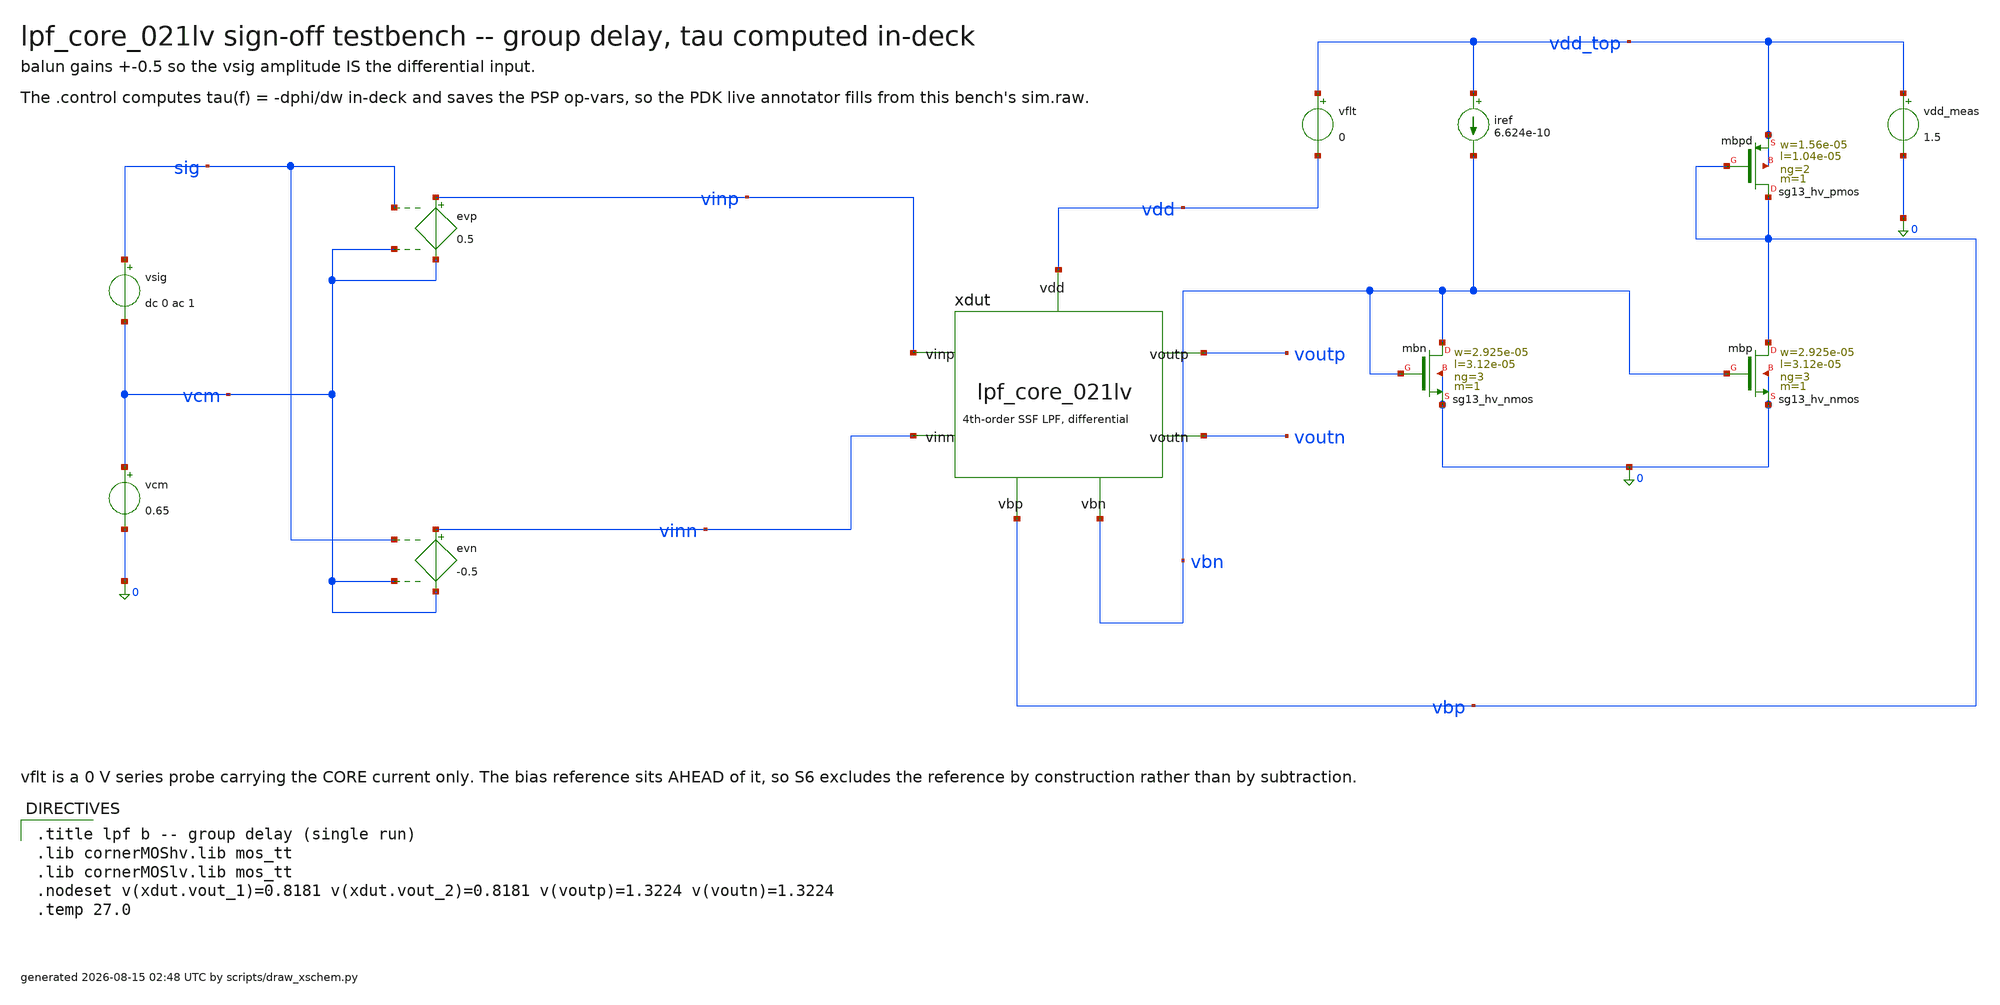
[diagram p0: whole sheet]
** sch_path: signoff/pre-pvt/schematic/lpf_tb_021lv_gd.sch
**.subckt lpf_tb_021lv_gd
vsig sig vcm dc 0 ac 1
vcm vcm 0 0.65
evp vinp vcm sig vcm 0.5
evn vinn vcm sig vcm -0.5
xdut vinp vinn voutp voutn vbn vbp vdd lpf_core_021lv
vflt vdd_top vdd 0
vdd_meas vdd_top 0 1.5
iref vdd_top vbn 6.624e-10
Xmbn vbn vbn 0 0 sg13_hv_nmos w=2.925e-05 l=3.12e-05 ng=3 m=1 mm_ok=1
Xmbp vbp vbn 0 0 sg13_hv_nmos w=2.925e-05 l=3.12e-05 ng=3 m=1 mm_ok=1
Xmbpd vbp vbp vdd_top vdd_top sg13_hv_pmos w=1.56e-05 l=1.04e-05 ng=2 m=1 mm_ok=1
**** begin user architecture code

.title lpf b -- group delay (single run)
.lib cornerMOShv.lib mos_tt
.lib cornerMOSlv.lib mos_tt
.nodeset v(xdut.vout_1)=0.8181 v(xdut.vout_2)=0.8181 v(voutp)=1.3224 v(voutn)=1.3224
.temp 27.0


.control
set filetype=binary
set appendwrite
save all @n.xdut.xm2.nsg13_lv_pmos[ids] @n.xdut.xm2.nsg13_lv_pmos[gm] @n.xdut.xm2.nsg13_lv_pmos[gds]
+ @n.xdut.xm2.nsg13_lv_pmos[gmb] @n.xdut.xm2.nsg13_lv_pmos[vgs] @n.xdut.xm2.nsg13_lv_pmos[vds] @n.xdut.xm2.nsg13_lv_pmos[vth]
+ @n.xdut.xm2.nsg13_lv_pmos[vdss] @n.xdut.xm2.nsg13_lv_pmos[cgg] @n.xdut.xm5.nsg13_lv_pmos[ids] @n.xdut.xm5.nsg13_lv_pmos[gm]
+ @n.xdut.xm5.nsg13_lv_pmos[gds] @n.xdut.xm5.nsg13_lv_pmos[gmb] @n.xdut.xm5.nsg13_lv_pmos[vgs] @n.xdut.xm5.nsg13_lv_pmos[vds]
+ @n.xdut.xm5.nsg13_lv_pmos[vth] @n.xdut.xm5.nsg13_lv_pmos[vdss] @n.xdut.xm5.nsg13_lv_pmos[cgg] @n.xdut.xm4.nsg13_hv_nmos[ids]
+ @n.xdut.xm4.nsg13_hv_nmos[gm] @n.xdut.xm4.nsg13_hv_nmos[gds] @n.xdut.xm4.nsg13_hv_nmos[gmb] @n.xdut.xm4.nsg13_hv_nmos[vgs]
+ @n.xdut.xm4.nsg13_hv_nmos[vds] @n.xdut.xm4.nsg13_hv_nmos[vth] @n.xdut.xm4.nsg13_hv_nmos[vdss] @n.xdut.xm4.nsg13_hv_nmos[cgg]
+ @n.xdut.xm8.nsg13_hv_nmos[ids] @n.xdut.xm8.nsg13_hv_nmos[gm] @n.xdut.xm8.nsg13_hv_nmos[gds] @n.xdut.xm8.nsg13_hv_nmos[gmb]
+ @n.xdut.xm8.nsg13_hv_nmos[vgs] @n.xdut.xm8.nsg13_hv_nmos[vds] @n.xdut.xm8.nsg13_hv_nmos[vth] @n.xdut.xm8.nsg13_hv_nmos[vdss]
+ @n.xdut.xm8.nsg13_hv_nmos[cgg] @n.xdut.xm9.nsg13_hv_nmos[ids] @n.xdut.xm9.nsg13_hv_nmos[gm] @n.xdut.xm9.nsg13_hv_nmos[gds]
+ @n.xdut.xm9.nsg13_hv_nmos[gmb] @n.xdut.xm9.nsg13_hv_nmos[vgs] @n.xdut.xm9.nsg13_hv_nmos[vds] @n.xdut.xm9.nsg13_hv_nmos[vth]
+ @n.xdut.xm9.nsg13_hv_nmos[vdss] @n.xdut.xm9.nsg13_hv_nmos[cgg] @n.xdut.xm10.nsg13_hv_nmos[ids] @n.xdut.xm10.nsg13_hv_nmos[gm]
+ @n.xdut.xm10.nsg13_hv_nmos[gds] @n.xdut.xm10.nsg13_hv_nmos[gmb] @n.xdut.xm10.nsg13_hv_nmos[vgs] @n.xdut.xm10.nsg13_hv_nmos[vds]
+ @n.xdut.xm10.nsg13_hv_nmos[vth] @n.xdut.xm10.nsg13_hv_nmos[vdss] @n.xdut.xm10.nsg13_hv_nmos[cgg] @n.xdut.xmst.nsg13_hv_pmos[ids]
+ @n.xdut.xmst.nsg13_hv_pmos[gm] @n.xdut.xmst.nsg13_hv_pmos[gds] @n.xdut.xmst.nsg13_hv_pmos[gmb] @n.xdut.xmst.nsg13_hv_pmos[vgs]
+ @n.xdut.xmst.nsg13_hv_pmos[vds] @n.xdut.xmst.nsg13_hv_pmos[vth] @n.xdut.xmst.nsg13_hv_pmos[vdss] @n.xdut.xmst.nsg13_hv_pmos[cgg]
+ @n.xdut.xmstn.nsg13_hv_pmos[ids] @n.xdut.xmstn.nsg13_hv_pmos[gm] @n.xdut.xmstn.nsg13_hv_pmos[gds] @n.xdut.xmstn.nsg13_hv_pmos[gmb]
+ @n.xdut.xmstn.nsg13_hv_pmos[vgs] @n.xdut.xmstn.nsg13_hv_pmos[vds] @n.xdut.xmstn.nsg13_hv_pmos[vth] @n.xdut.xmstn.nsg13_hv_pmos[vdss]
+ @n.xdut.xmstn.nsg13_hv_pmos[cgg] @n.xdut.xm0.nsg13_hv_pmos[ids] @n.xdut.xm0.nsg13_hv_pmos[gm] @n.xdut.xm0.nsg13_hv_pmos[gds]
+ @n.xdut.xm0.nsg13_hv_pmos[gmb] @n.xdut.xm0.nsg13_hv_pmos[vgs] @n.xdut.xm0.nsg13_hv_pmos[vds] @n.xdut.xm0.nsg13_hv_pmos[vth]
+ @n.xdut.xm0.nsg13_hv_pmos[vdss] @n.xdut.xm0.nsg13_hv_pmos[cgg] @n.xdut.xm1.nsg13_hv_pmos[ids] @n.xdut.xm1.nsg13_hv_pmos[gm]
+ @n.xdut.xm1.nsg13_hv_pmos[gds] @n.xdut.xm1.nsg13_hv_pmos[gmb] @n.xdut.xm1.nsg13_hv_pmos[vgs] @n.xdut.xm1.nsg13_hv_pmos[vds]
+ @n.xdut.xm1.nsg13_hv_pmos[vth] @n.xdut.xm1.nsg13_hv_pmos[vdss] @n.xdut.xm1.nsg13_hv_pmos[cgg] @n.xdut.xm14.nsg13_hv_pmos[ids]
+ @n.xdut.xm14.nsg13_hv_pmos[gm] @n.xdut.xm14.nsg13_hv_pmos[gds] @n.xdut.xm14.nsg13_hv_pmos[gmb] @n.xdut.xm14.nsg13_hv_pmos[vgs]
+ @n.xdut.xm14.nsg13_hv_pmos[vds] @n.xdut.xm14.nsg13_hv_pmos[vth] @n.xdut.xm14.nsg13_hv_pmos[vdss] @n.xdut.xm14.nsg13_hv_pmos[cgg]
+ @n.xdut.xm15.nsg13_hv_pmos[ids] @n.xdut.xm15.nsg13_hv_pmos[gm] @n.xdut.xm15.nsg13_hv_pmos[gds] @n.xdut.xm15.nsg13_hv_pmos[gmb]
+ @n.xdut.xm15.nsg13_hv_pmos[vgs] @n.xdut.xm15.nsg13_hv_pmos[vds] @n.xdut.xm15.nsg13_hv_pmos[vth] @n.xdut.xm15.nsg13_hv_pmos[vdss]
+ @n.xdut.xm15.nsg13_hv_pmos[cgg]
op
write sim.raw
ac dec 50 0.1 1000
let hdiff = v(voutp) - v(voutn)
let hdb = db(mag(hdiff))
let dc_db = hdb[0]
let ph = cph(hdiff)
let gd = -deriv(ph) / (2 * pi)
let gd_dc_ms = gd[0] * 1e3
let gd_max_ms = vecmax(gd) * 1e3
let hrel = hdb - dc_db
meas ac fc_hz when hrel = -3 fall = 1
print dc_db gd_dc_ms gd_max_ms
write sim.raw hdiff ph gd frequency
.endc

**** end user architecture code
**.ends

* expanding   symbol:  lpf_core_021lv.sym # of pins=7
** sym_path: signoff/schematic/lpf_core_021lv.sym
** sch_path: signoff/schematic/lpf_core_021lv.sch
.subckt lpf_core_021lv vinp vinn voutp voutn vbn vbp vdd
*.ipin vinp
*.ipin vinn
*.opin voutp
*.opin voutn
*.ipin vdd
*.ipin vbn
*.ipin vbp
Xm2 net2 vinp vout_1 vout_1 sg13_lv_pmos w=1.56e-05 l=1.04e-05 ng=2 m=1 mm_ok=1
Xm5 net3 vinn vout_2 vout_2 sg13_lv_pmos w=1.56e-05 l=1.04e-05 ng=2 m=1 mm_ok=1
Xm4 vout_1 net2 0 0 sg13_hv_nmos w=7.8e-06 l=5.2e-06 ng=1 m=1 mm_ok=1
Xm8 vout_2 net3 0 0 sg13_hv_nmos w=7.8e-06 l=5.2e-06 ng=1 m=1 mm_ok=1
Xm9 net2 vbn 0 0 sg13_hv_nmos w=2.925e-05 l=3.12e-05 ng=3 m=1 mm_ok=1
Xm10 net3 vbn 0 0 sg13_hv_nmos w=2.925e-05 l=3.12e-05 ng=3 m=1 mm_ok=1
Xmst vout_1 vbn net4 net4 sg13_hv_pmos w=1.62e-06 l=1.092e-05 ng=1 m=1 mm_ok=1
Xmstn vout_2 vbn net1 net1 sg13_hv_pmos w=1.62e-06 l=1.092e-05 ng=1 m=1 mm_ok=1
Xm0 net4 vout_1 voutp voutp sg13_hv_pmos w=1.56e-05 l=1.04e-05 ng=2 m=1 mm_ok=1
Xm1 net1 vout_2 voutn voutn sg13_hv_pmos w=1.56e-05 l=1.04e-05 ng=2 m=1 mm_ok=1
Xm14 voutp net4 vdd vdd sg13_hv_pmos w=8.085e-06 l=1.56e-05 ng=1 m=1 mm_ok=1
Xm15 voutn net1 vdd vdd sg13_hv_pmos w=8.085e-06 l=1.56e-05 ng=1 m=1 mm_ok=1
c13 net2 vout_1 6.58174e-12 m=1
c17 net3 vout_2 6.58174e-12 m=1
c19 vout_2 vout_1 2.65642e-11 m=1
c1 voutp net4 5.18878e-11 m=1
c10 voutn net1 5.18878e-11 m=1
c12 voutn voutp 2.04984e-11 m=1
.ends

.end
